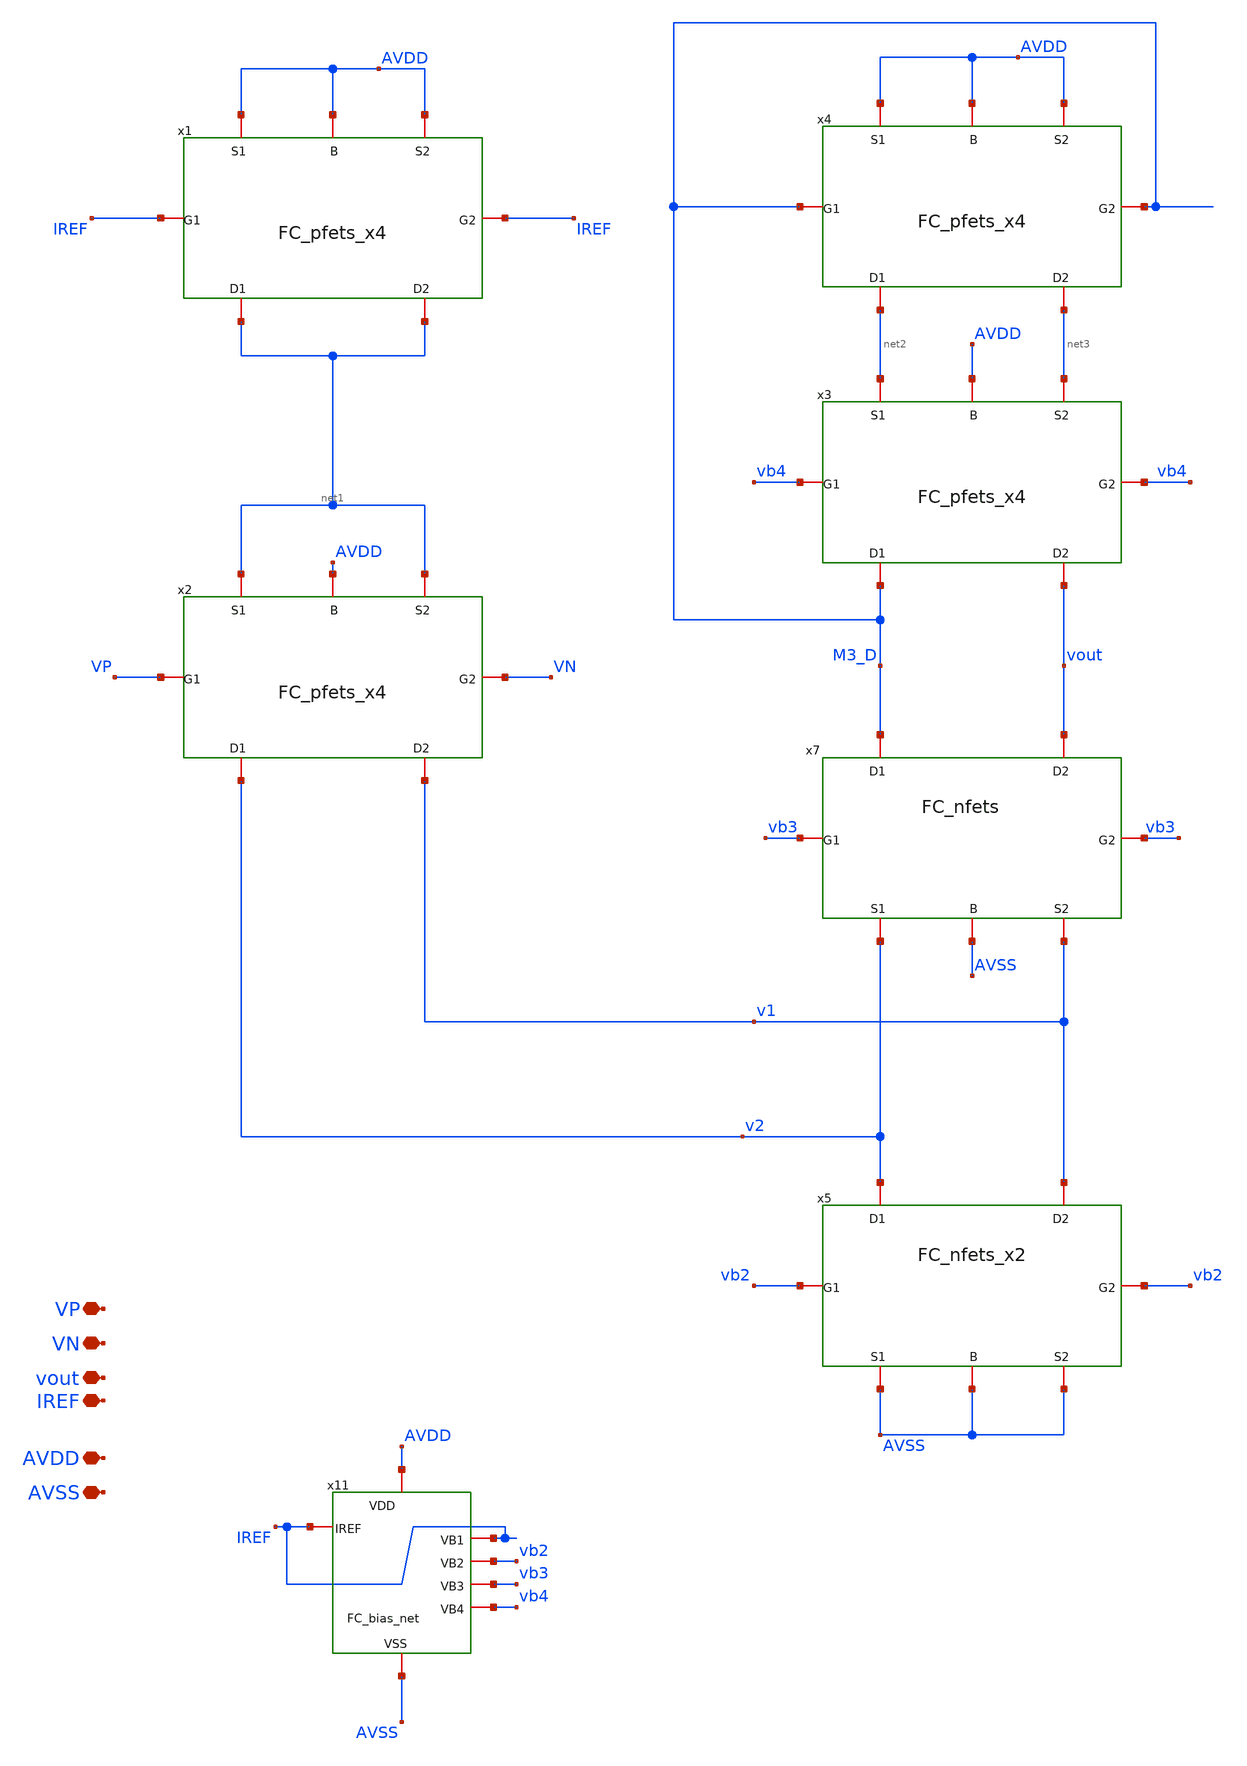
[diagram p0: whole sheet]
** sch_path: Voltage_Reference/LDO/Folded/FoldedCascode.sch
**.subckt FoldedCascode AVDD AVSS vout VP VN IREF
*.iopin AVDD
*.iopin AVSS
*.iopin vout
*.iopin VP
*.iopin VN
*.iopin IREF
x7 v2 v1 M3_D vout vb3 vb3 AVSS FC_nfets
x5 AVSS AVSS v2 v1 vb2 vb2 AVSS FC_nfets_x2
x1 AVDD AVDD net1 net1 IREF IREF AVDD FC_pfets_x4
x2 net1 net1 v2 v1 VP VN AVDD FC_pfets_x4
x3 net2 net3 M3_D vout vb4 vb4 AVDD FC_pfets_x4
x4 AVDD AVDD net2 net3 M3_D M3_D AVDD FC_pfets_x4
x11 IREF IREF vb2 vb3 vb4 AVDD AVSS FC_bias_net
**.ends
.end
